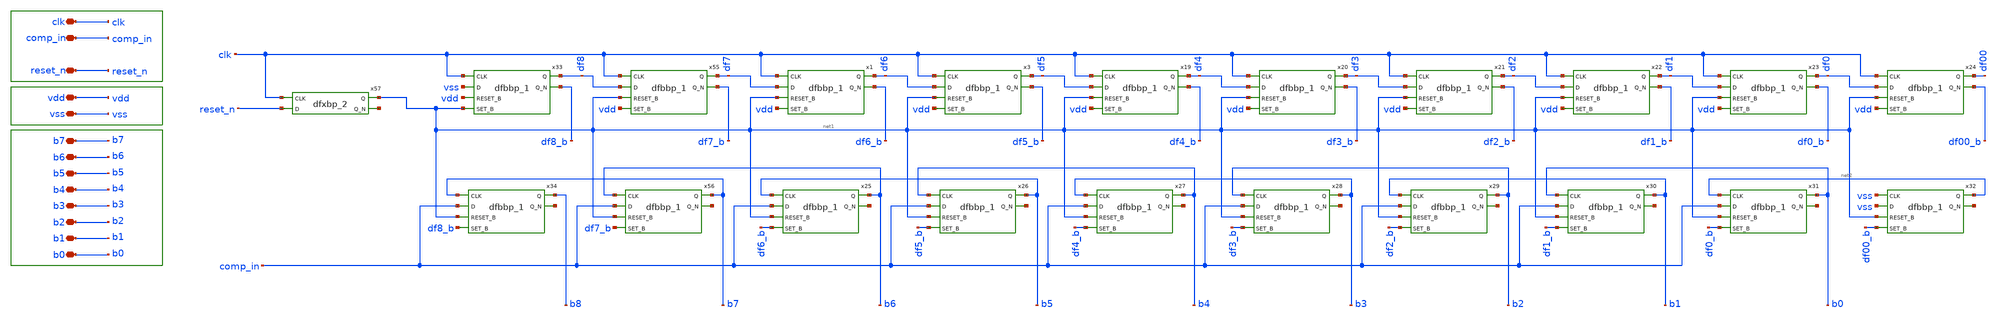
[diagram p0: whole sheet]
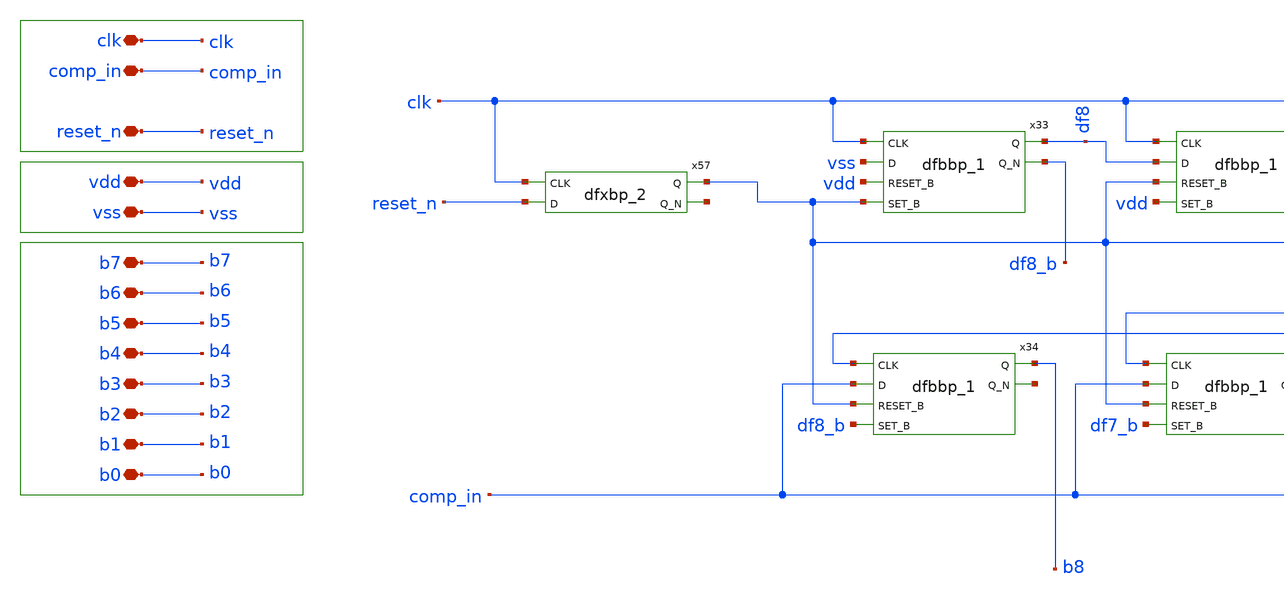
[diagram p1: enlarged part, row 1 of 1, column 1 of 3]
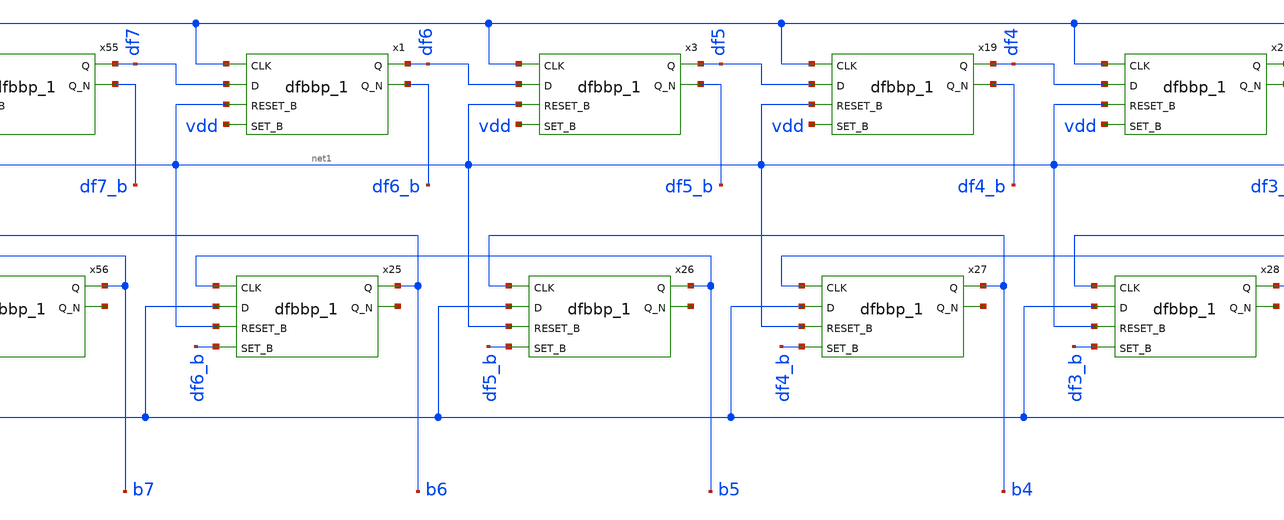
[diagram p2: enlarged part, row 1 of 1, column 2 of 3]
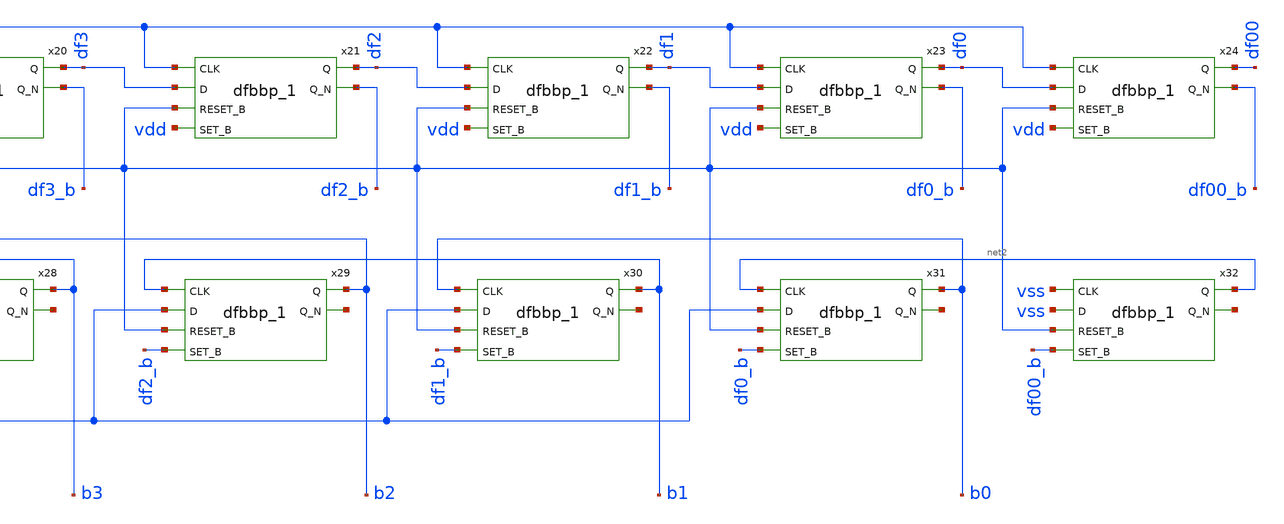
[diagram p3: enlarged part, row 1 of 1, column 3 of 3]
** sch_path: xschem/sar_logic/sarlogic.sch
**.subckt sarlogic vdd clk b7 b6 b5 b4 b3 b2 b1 b0 comp_in vss reset_n
*.iopin vdd
*.iopin clk
*.iopin b7
*.iopin b6
*.iopin b5
*.iopin b4
*.iopin b3
*.iopin b2
*.iopin b1
*.iopin b0
*.iopin comp_in
*.iopin vss
*.iopin reset_n
x1 clk df7 net1 vdd vss vss vdd vdd df6 df6_b sky130_fd_sc_hd__dfbbp_1
x3 clk df6 net1 vdd vss vss vdd vdd df5 df5_b sky130_fd_sc_hd__dfbbp_1
x19 clk df5 net1 vdd vss vss vdd vdd df4 df4_b sky130_fd_sc_hd__dfbbp_1
x20 clk df4 net1 vdd vss vss vdd vdd df3 df3_b sky130_fd_sc_hd__dfbbp_1
x21 clk df3 net1 vdd vss vss vdd vdd df2 df2_b sky130_fd_sc_hd__dfbbp_1
x22 clk df2 net1 vdd vss vss vdd vdd df1 df1_b sky130_fd_sc_hd__dfbbp_1
x23 clk df1 net1 vdd vss vss vdd vdd df0 df0_b sky130_fd_sc_hd__dfbbp_1
x24 clk df0 net1 vdd vss vss vdd vdd df00 df00_b sky130_fd_sc_hd__dfbbp_1
x25 b5 comp_in net1 df6_b vss vss vdd vdd b6 net3 sky130_fd_sc_hd__dfbbp_1
x26 b4 comp_in net1 df5_b vss vss vdd vdd b5 net4 sky130_fd_sc_hd__dfbbp_1
x27 b3 comp_in net1 df4_b vss vss vdd vdd b4 net5 sky130_fd_sc_hd__dfbbp_1
x28 b2 comp_in net1 df3_b vss vss vdd vdd b3 net6 sky130_fd_sc_hd__dfbbp_1
x29 b1 comp_in net1 df2_b vss vss vdd vdd b2 net7 sky130_fd_sc_hd__dfbbp_1
x30 b0 comp_in net1 df1_b vss vss vdd vdd b1 net8 sky130_fd_sc_hd__dfbbp_1
x31 net2 comp_in net1 df0_b vss vss vdd vdd b0 net9 sky130_fd_sc_hd__dfbbp_1
x32 vss vss net1 df00_b vss vss vdd vdd net2 net10 sky130_fd_sc_hd__dfbbp_1
x33 clk vss vdd net1 vss vss vdd vdd df8 df8_b sky130_fd_sc_hd__dfbbp_1
x34 b7 comp_in net1 df8_b vss vss vdd vdd b8 net11 sky130_fd_sc_hd__dfbbp_1
x55 clk df8 net1 vdd vss vss vdd vdd df7 df7_b sky130_fd_sc_hd__dfbbp_1
x56 b6 comp_in net1 df7_b vss vss vdd vdd b7 net12 sky130_fd_sc_hd__dfbbp_1
x57 clk reset_n vss vss vdd vdd net1 net13 sky130_fd_sc_hd__dfxbp_2
**.ends
.end
